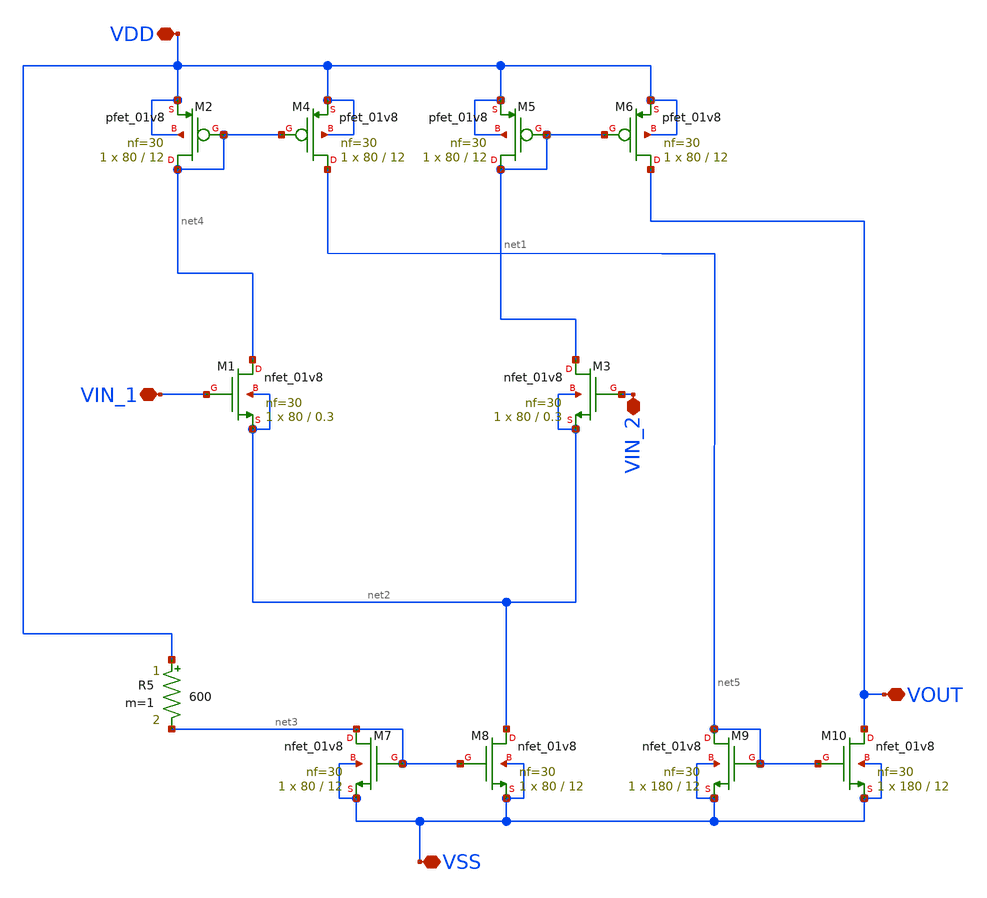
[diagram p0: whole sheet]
** sch_path: xschem/transcond.sch
**.subckt transcond VIN_1 VIN_2 VOUT VSS VDD
*.iopin VIN_1
*.iopin VIN_2
*.iopin VOUT
*.iopin VSS
*.iopin VDD
XM3 net1 VIN_2 net2 net2 sky130_fd_pr__nfet_01v8 L=0.3 W=80 nf=30 ad='int((nf+1)/2) * W/nf * 0.29' as='int((nf+2)/2) * W/nf * 0.29'
+ pd='2*int((nf+1)/2) * (W/nf + 0.29)' ps='2*int((nf+2)/2) * (W/nf + 0.29)' nrd='0.29 / W' nrs='0.29 / W'
+ sa=0 sb=0 sd=0 mult=1 m=1
XM7 net3 net3 VSS VSS sky130_fd_pr__nfet_01v8 L=12 W=80 nf=30 ad='int((nf+1)/2) * W/nf * 0.29' as='int((nf+2)/2) * W/nf * 0.29'
+ pd='2*int((nf+1)/2) * (W/nf + 0.29)' ps='2*int((nf+2)/2) * (W/nf + 0.29)' nrd='0.29 / W' nrs='0.29 / W'
+ sa=0 sb=0 sd=0 mult=1 m=1
XM8 net2 net3 VSS VSS sky130_fd_pr__nfet_01v8 L=12 W=80 nf=30 ad='int((nf+1)/2) * W/nf * 0.29' as='int((nf+2)/2) * W/nf * 0.29'
+ pd='2*int((nf+1)/2) * (W/nf + 0.29)' ps='2*int((nf+2)/2) * (W/nf + 0.29)' nrd='0.29 / W' nrs='0.29 / W'
+ sa=0 sb=0 sd=0 mult=1 m=1
XM5 net1 net1 VDD VDD sky130_fd_pr__pfet_01v8 L=12 W=80 nf=30 ad='int((nf+1)/2) * W/nf * 0.29' as='int((nf+2)/2) * W/nf * 0.29'
+ pd='2*int((nf+1)/2) * (W/nf + 0.29)' ps='2*int((nf+2)/2) * (W/nf + 0.29)' nrd='0.29 / W' nrs='0.29 / W'
+ sa=0 sb=0 sd=0 mult=1 m=1
XM6 VOUT net1 VDD VDD sky130_fd_pr__pfet_01v8 L=12 W=80 nf=30 ad='int((nf+1)/2) * W/nf * 0.29' as='int((nf+2)/2) * W/nf * 0.29'
+ pd='2*int((nf+1)/2) * (W/nf + 0.29)' ps='2*int((nf+2)/2) * (W/nf + 0.29)' nrd='0.29 / W' nrs='0.29 / W'
+ sa=0 sb=0 sd=0 mult=1 m=1
R5 VDD net3 600 m=1
XM2 net4 net4 VDD VDD sky130_fd_pr__pfet_01v8 L=12 W=80 nf=30 ad='int((nf+1)/2) * W/nf * 0.29' as='int((nf+2)/2) * W/nf * 0.29'
+ pd='2*int((nf+1)/2) * (W/nf + 0.29)' ps='2*int((nf+2)/2) * (W/nf + 0.29)' nrd='0.29 / W' nrs='0.29 / W'
+ sa=0 sb=0 sd=0 mult=1 m=1
XM4 net5 net4 VDD VDD sky130_fd_pr__pfet_01v8 L=12 W=80 nf=30 ad='int((nf+1)/2) * W/nf * 0.29' as='int((nf+2)/2) * W/nf * 0.29'
+ pd='2*int((nf+1)/2) * (W/nf + 0.29)' ps='2*int((nf+2)/2) * (W/nf + 0.29)' nrd='0.29 / W' nrs='0.29 / W'
+ sa=0 sb=0 sd=0 mult=1 m=1
XM9 net5 net5 VSS VSS sky130_fd_pr__nfet_01v8 L=12 W=180 nf=30 ad='int((nf+1)/2) * W/nf * 0.29' as='int((nf+2)/2) * W/nf * 0.29'
+ pd='2*int((nf+1)/2) * (W/nf + 0.29)' ps='2*int((nf+2)/2) * (W/nf + 0.29)' nrd='0.29 / W' nrs='0.29 / W'
+ sa=0 sb=0 sd=0 mult=1 m=1
XM10 VOUT net5 VSS VSS sky130_fd_pr__nfet_01v8 L=12 W=180 nf=30 ad='int((nf+1)/2) * W/nf * 0.29' as='int((nf+2)/2) * W/nf * 0.29'
+ pd='2*int((nf+1)/2) * (W/nf + 0.29)' ps='2*int((nf+2)/2) * (W/nf + 0.29)' nrd='0.29 / W' nrs='0.29 / W'
+ sa=0 sb=0 sd=0 mult=1 m=1
XM1 net4 VIN_1 net2 net2 sky130_fd_pr__nfet_01v8 L=0.3 W=80 nf=30 ad='int((nf+1)/2) * W/nf * 0.29' as='int((nf+2)/2) * W/nf * 0.29'
+ pd='2*int((nf+1)/2) * (W/nf + 0.29)' ps='2*int((nf+2)/2) * (W/nf + 0.29)' nrd='0.29 / W' nrs='0.29 / W'
+ sa=0 sb=0 sd=0 mult=1 m=1
**.ends
.end
